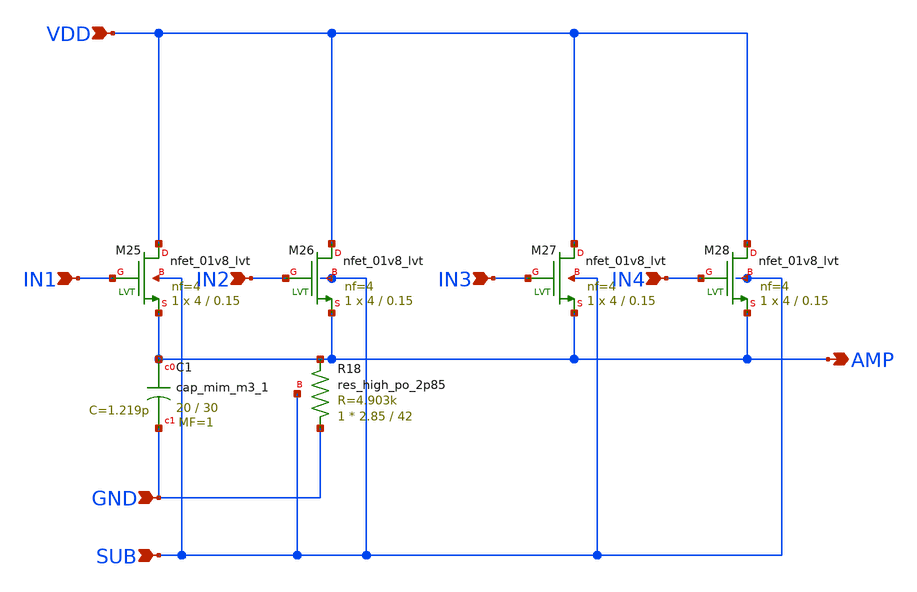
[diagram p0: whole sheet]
** sch_path: design/vco/1.7G~10G/schematic/amp_dec.sch
**.subckt amp_dec VDD SUB GND IN1 IN2 IN3 IN4 AMP
*.ipin VDD
*.ipin SUB
*.ipin GND
*.ipin IN1
*.ipin IN2
*.ipin IN3
*.ipin IN4
*.opin AMP
XM25 VDD IN1 AMP SUB sky130_fd_pr__nfet_01v8_lvt L=0.15 W=4 nf=4 ad='int((nf+1)/2) * W/nf * 0.29' as='int((nf+2)/2) * W/nf * 0.29'
+ pd='2*int((nf+1)/2) * (W/nf + 0.29)' ps='2*int((nf+2)/2) * (W/nf + 0.29)' nrd='0.29 / W' nrs='0.29 / W'
+ sa=0 sb=0 sd=0 mult=1 m=1
XC1 AMP GND sky130_fd_pr__cap_mim_m3_1 W=20 L=30 MF=1 m=1
XM26 VDD IN2 AMP SUB sky130_fd_pr__nfet_01v8_lvt L=0.15 W=4 nf=4 ad='int((nf+1)/2) * W/nf * 0.29' as='int((nf+2)/2) * W/nf * 0.29'
+ pd='2*int((nf+1)/2) * (W/nf + 0.29)' ps='2*int((nf+2)/2) * (W/nf + 0.29)' nrd='0.29 / W' nrs='0.29 / W'
+ sa=0 sb=0 sd=0 mult=1 m=1
XM27 VDD IN3 AMP SUB sky130_fd_pr__nfet_01v8_lvt L=0.15 W=4 nf=4 ad='int((nf+1)/2) * W/nf * 0.29' as='int((nf+2)/2) * W/nf * 0.29'
+ pd='2*int((nf+1)/2) * (W/nf + 0.29)' ps='2*int((nf+2)/2) * (W/nf + 0.29)' nrd='0.29 / W' nrs='0.29 / W'
+ sa=0 sb=0 sd=0 mult=1 m=1
XM28 VDD IN4 AMP SUB sky130_fd_pr__nfet_01v8_lvt L=0.15 W=4 nf=4 ad='int((nf+1)/2) * W/nf * 0.29' as='int((nf+2)/2) * W/nf * 0.29'
+ pd='2*int((nf+1)/2) * (W/nf + 0.29)' ps='2*int((nf+2)/2) * (W/nf + 0.29)' nrd='0.29 / W' nrs='0.29 / W'
+ sa=0 sb=0 sd=0 mult=1 m=1
XR18 GND AMP SUB sky130_fd_pr__res_high_po_2p85 L=42 mult=1 m=1
**.ends
.end
